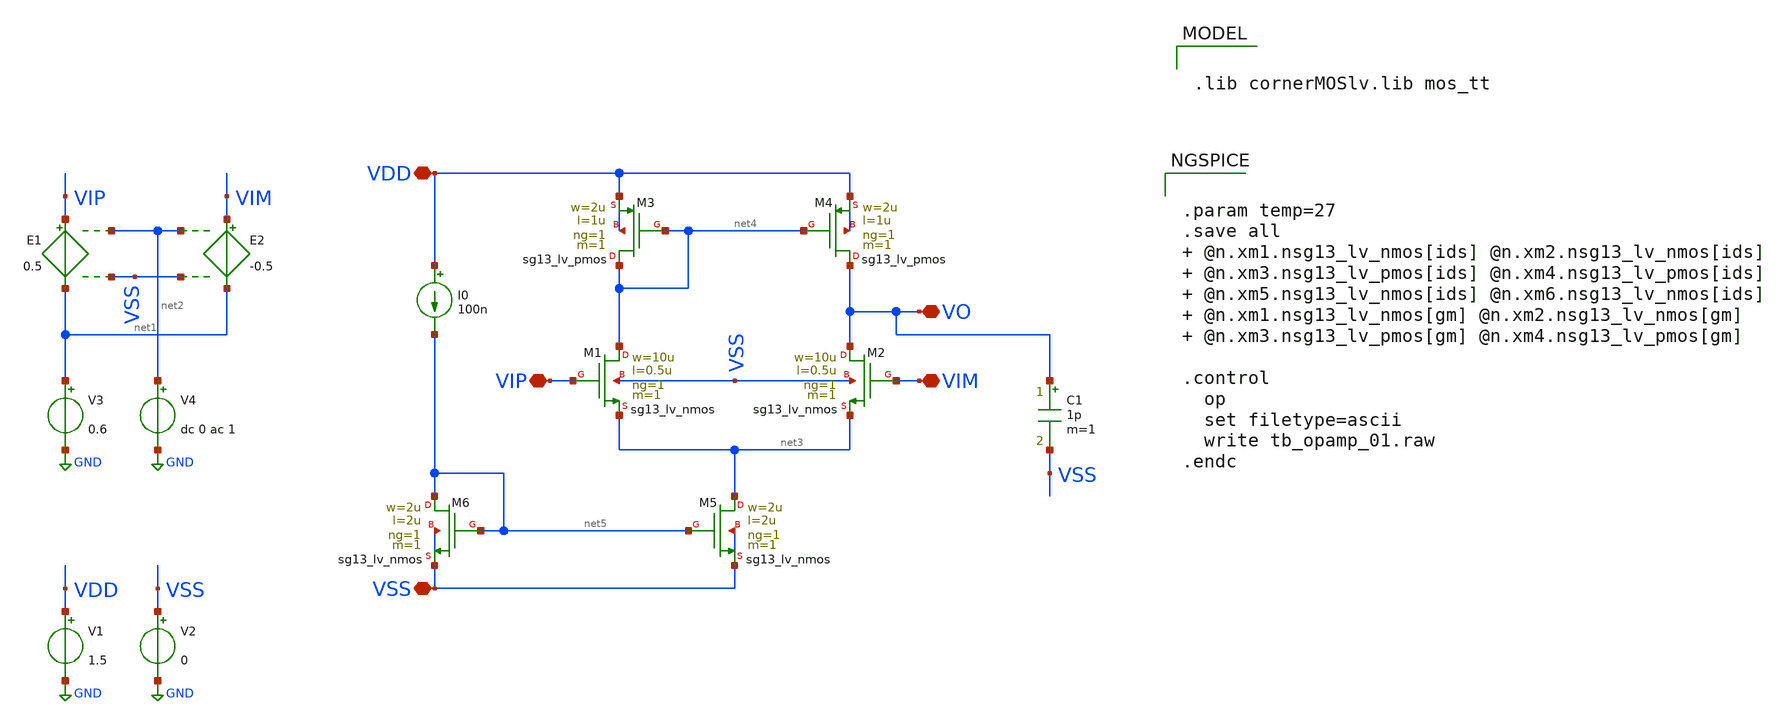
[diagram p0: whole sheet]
** sch_path: analog/tb/tb_amp_01.sch
**.subckt tb_amp_01 VIM VIP VSS VDD VO
*.iopin VIM
*.iopin VIP
*.iopin VSS
*.iopin VDD
*.iopin VO
C1 VO VSS 1p m=1
V1 VDD GND 1.5
E1 VIP net1 net2 VSS 0.5
V2 VSS GND 0
E2 VIM net1 net2 VSS -0.5
V3 net1 GND 0.6
V4 net2 GND dc 0 ac 1
XM1 net4 VIP net3 VSS sg13_lv_nmos w=10u l=0.5u ng=1 m=1 mm_ok=1
XM2 VO VIM net3 VSS sg13_lv_nmos w=10u l=0.5u ng=1 m=1 mm_ok=1
XM3 net4 net4 VDD VDD sg13_lv_pmos w=2u l=1u ng=1 m=1 mm_ok=1
XM4 VO net4 VDD VDD sg13_lv_pmos w=2u l=1u ng=1 m=1 mm_ok=1
XM5 net3 net5 VSS VSS sg13_lv_nmos w=2u l=2u ng=1 m=1 mm_ok=1
XM6 net5 net5 VSS VSS sg13_lv_nmos w=2u l=2u ng=1 m=1 mm_ok=1
I0 VDD net5 100n
**** begin user architecture code


.param temp=27
.save all  @n.xm1.nsg13_lv_nmos[ids] @n.xm2.nsg13_lv_nmos[ids]  @n.xm3.nsg13_lv_pmos[ids] @n.xm4.nsg13_lv_pmos[ids]  @n.xm5.nsg13_lv_nmos[ids] @n.xm6.nsg13_lv_nmos[ids]  @n.xm1.nsg13_lv_nmos[gm] @n.xm2.nsg13_lv_nmos[gm]  @n.xm3.nsg13_lv_pmos[gm] @n.xm4.nsg13_lv_pmos[gm]

.control
  op
  set filetype=ascii
  write tb_opamp_01.raw
.endc




.lib cornerMOSlv.lib mos_tt


**** end user architecture code
**.ends
.GLOBAL GND
.end
